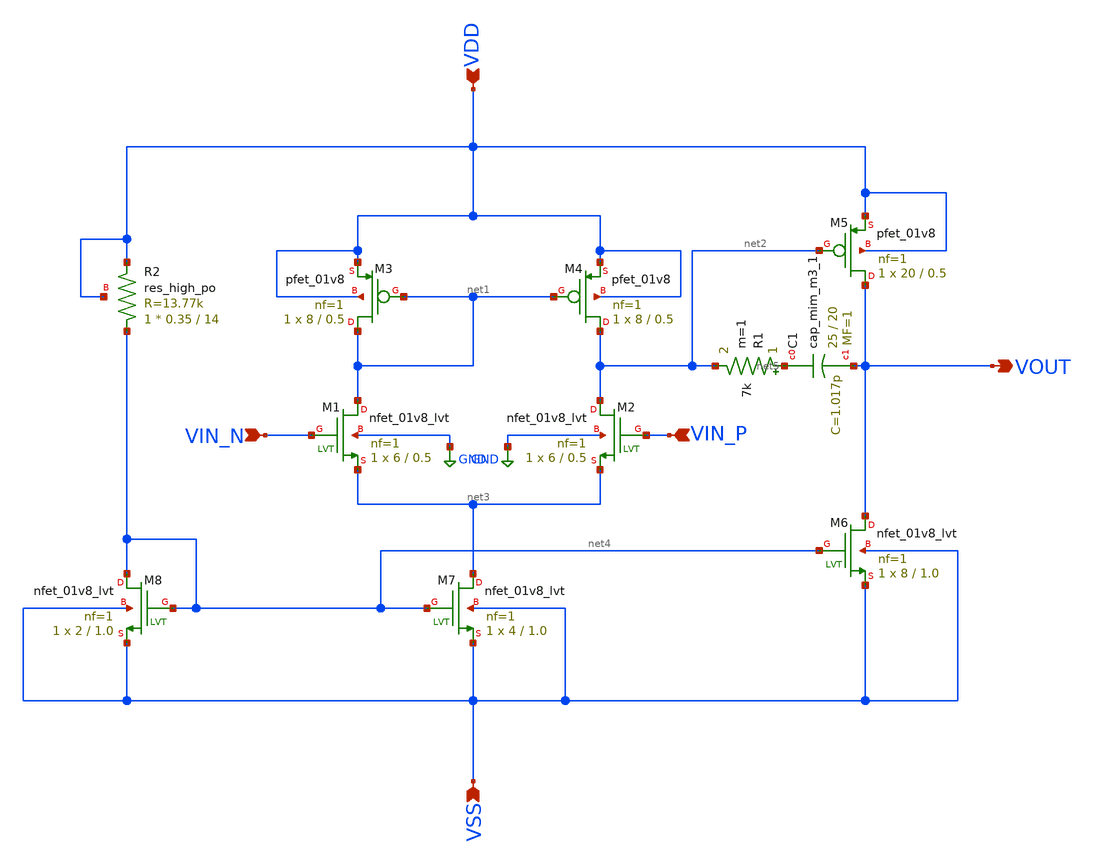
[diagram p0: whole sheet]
** sch_path: analog/schematics/opamp_single_stage.sch
**.subckt opamp_single_stage VDD VIN_P VSS VOUT VIN_N
*.ipin VDD
*.ipin VIN_P
*.ipin VSS
*.opin VOUT
*.ipin VIN_N
XM4 net2 net1 VDD VDD sky130_fd_pr__pfet_01v8 L=0.5 W=8 nf=1 ad='int((nf+1)/2) * W/nf * 0.29' as='int((nf+2)/2) * W/nf * 0.29'
+ pd='2*int((nf+1)/2) * (W/nf + 0.29)' ps='2*int((nf+2)/2) * (W/nf + 0.29)' nrd='0.29 / W' nrs='0.29 / W'
+ sa=0 sb=0 sd=0 mult=1 m=1
XM3 net1 net1 VDD VDD sky130_fd_pr__pfet_01v8 L=0.5 W=8 nf=1 ad='int((nf+1)/2) * W/nf * 0.29' as='int((nf+2)/2) * W/nf * 0.29'
+ pd='2*int((nf+1)/2) * (W/nf + 0.29)' ps='2*int((nf+2)/2) * (W/nf + 0.29)' nrd='0.29 / W' nrs='0.29 / W'
+ sa=0 sb=0 sd=0 mult=1 m=1
XM1 net1 VIN_N net3 GND sky130_fd_pr__nfet_01v8_lvt L=0.5 W=6 nf=1 ad='int((nf+1)/2) * W/nf * 0.29' as='int((nf+2)/2) * W/nf * 0.29'
+ pd='2*int((nf+1)/2) * (W/nf + 0.29)' ps='2*int((nf+2)/2) * (W/nf + 0.29)' nrd='0.29 / W' nrs='0.29 / W'
+ sa=0 sb=0 sd=0 mult=1 m=1
XM2 net2 VIN_P net3 GND sky130_fd_pr__nfet_01v8_lvt L=0.5 W=6 nf=1 ad='int((nf+1)/2) * W/nf * 0.29' as='int((nf+2)/2) * W/nf * 0.29'
+ pd='2*int((nf+1)/2) * (W/nf + 0.29)' ps='2*int((nf+2)/2) * (W/nf + 0.29)' nrd='0.29 / W' nrs='0.29 / W'
+ sa=0 sb=0 sd=0 mult=1 m=1
XM5 VOUT net2 VDD VDD sky130_fd_pr__pfet_01v8 L=0.5 W=20 nf=1 ad='int((nf+1)/2) * W/nf * 0.29' as='int((nf+2)/2) * W/nf * 0.29'
+ pd='2*int((nf+1)/2) * (W/nf + 0.29)' ps='2*int((nf+2)/2) * (W/nf + 0.29)' nrd='0.29 / W' nrs='0.29 / W'
+ sa=0 sb=0 sd=0 mult=1 m=1
XC1 net5 VOUT sky130_fd_pr__cap_mim_m3_1 W=25 L=20 MF=1 m=1
XM8 net4 net4 VSS VSS sky130_fd_pr__nfet_01v8_lvt L=1.0 W=2 nf=1 ad='int((nf+1)/2) * W/nf * 0.29' as='int((nf+2)/2) * W/nf * 0.29'
+ pd='2*int((nf+1)/2) * (W/nf + 0.29)' ps='2*int((nf+2)/2) * (W/nf + 0.29)' nrd='0.29 / W' nrs='0.29 / W'
+ sa=0 sb=0 sd=0 mult=1 m=1
XM7 net3 net4 VSS VSS sky130_fd_pr__nfet_01v8_lvt L=1.0 W=4 nf=1 ad='int((nf+1)/2) * W/nf * 0.29' as='int((nf+2)/2) * W/nf * 0.29'
+ pd='2*int((nf+1)/2) * (W/nf + 0.29)' ps='2*int((nf+2)/2) * (W/nf + 0.29)' nrd='0.29 / W' nrs='0.29 / W'
+ sa=0 sb=0 sd=0 mult=1 m=1
XM6 VOUT net4 VSS VSS sky130_fd_pr__nfet_01v8_lvt L=1.0 W=8 nf=1 ad='int((nf+1)/2) * W/nf * 0.29' as='int((nf+2)/2) * W/nf * 0.29'
+ pd='2*int((nf+1)/2) * (W/nf + 0.29)' ps='2*int((nf+2)/2) * (W/nf + 0.29)' nrd='0.29 / W' nrs='0.29 / W'
+ sa=0 sb=0 sd=0 mult=1 m=1
R1 net5 net2 7k m=1
XR2 net4 VDD VDD sky130_fd_pr__res_high_po W=0.35 L=14 mult=1 m=1
**.ends
.GLOBAL GND
.end
